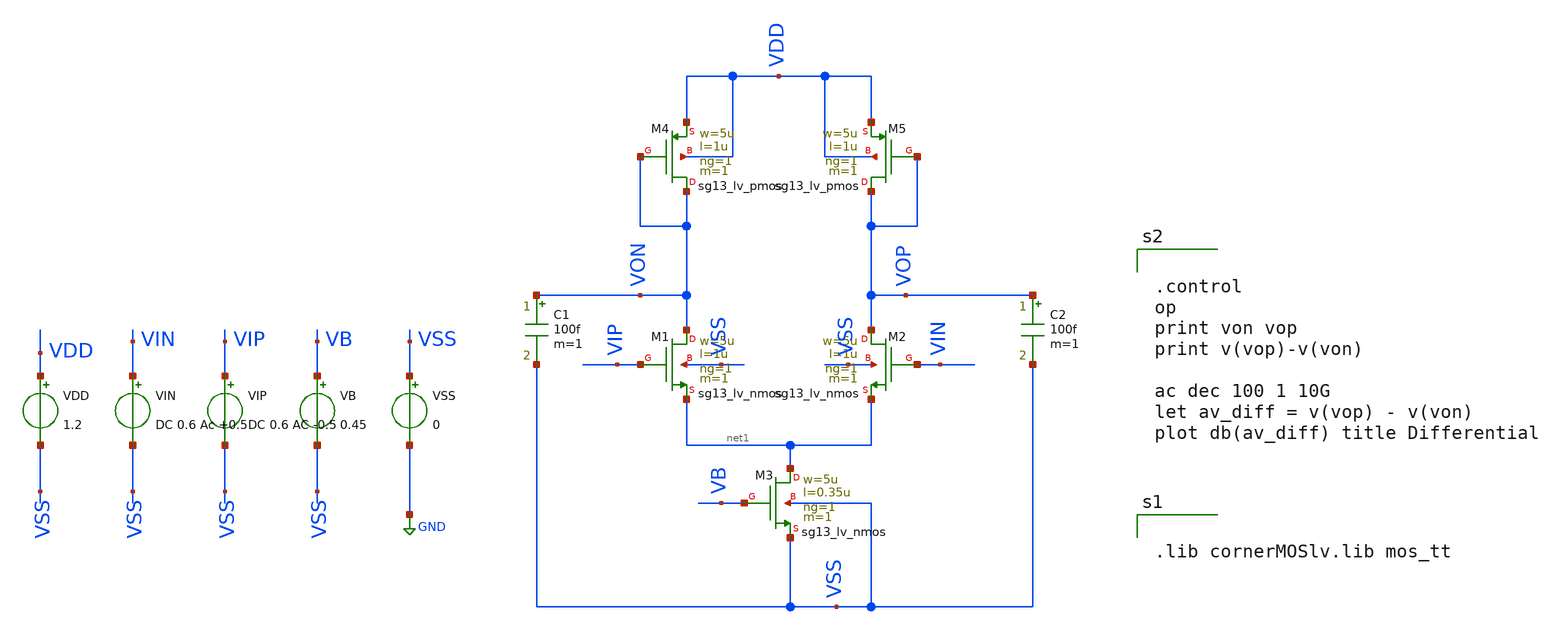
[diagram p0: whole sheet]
** sch_path: BTDay4-Ex/Ex2_Lecture4.sch
**.subckt Ex2_Lecture4
XM1 VON VIP net1 VSS sg13_lv_nmos w=5u l=1u ng=1 m=1 mm_ok=1
XM2 VOP VIN net1 VSS sg13_lv_nmos w=5u l=1u ng=1 m=1 mm_ok=1
XM3 net1 VB VSS VSS sg13_lv_nmos w=5u l=0.35u ng=1 m=1 mm_ok=1
VDD VDD VSS 1.2
VIN VIN VSS DC 0.6 Ac +0.5
VIP VIP VSS DC 0.6 AC -0.5
VB VB VSS 0.45
VSS VSS GND 0
C1 VON VSS 100f m=1
C2 VOP VSS 100f m=1
XM4 VON VON VDD VDD sg13_lv_pmos w=5u l=1u ng=1 m=1 mm_ok=1
XM5 VOP VOP VDD VDD sg13_lv_pmos w=5u l=1u ng=1 m=1 mm_ok=1
**** begin user architecture code


.lib cornerMOSlv.lib mos_tt




.control
op
print von vop
print v(vop)-v(von)

ac dec 100 1 10G
let av_diff = v(vop) - v(von)
plot db(av_diff) title Differential

**** end user architecture code
**.ends
.GLOBAL GND
.end
